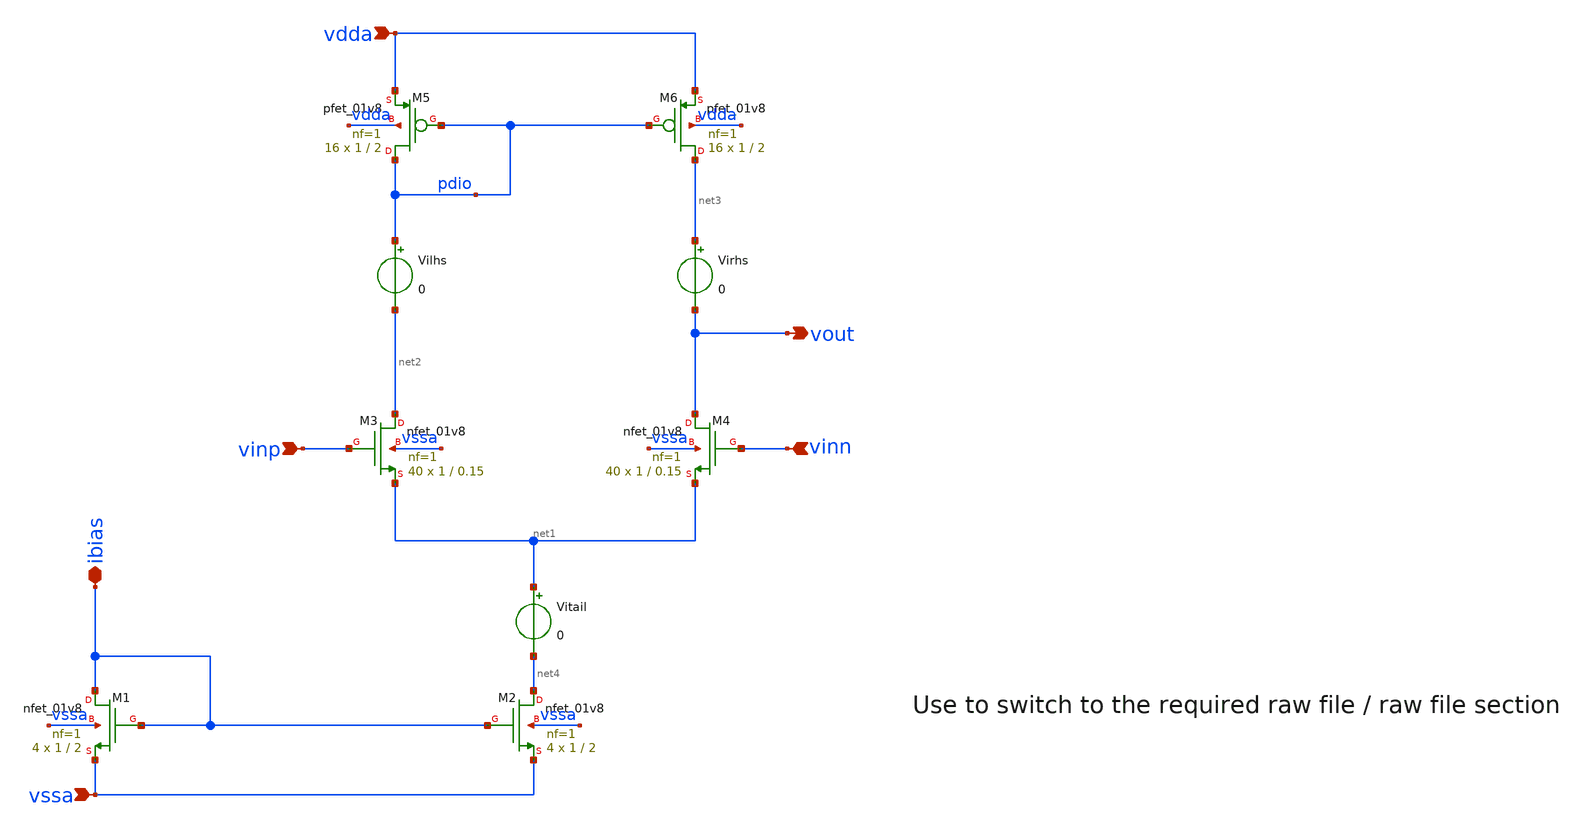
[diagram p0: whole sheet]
** sch_path: Analysing_DCOPs_in_xschem_ngpisce_in_SW130/OTA_DCOP2.sch
**.subckt OTA_DCOP2 ibias vdda vssa vinp vinn vout
*.iopin ibias
*.ipin vdda
*.ipin vssa
*.ipin vinp
*.ipin vinn
*.opin vout
XM3 net2 vinp net1 vssa sky130_fd_pr__nfet_01v8 L=0.15 W=1 nf=1 ad='int((nf+1)/2) * W/nf * 0.29' as='int((nf+2)/2) * W/nf * 0.29'
+ pd='2*int((nf+1)/2) * (W/nf + 0.29)' ps='2*int((nf+2)/2) * (W/nf + 0.29)' nrd='0.29 / W' nrs='0.29 / W'
+ sa=0 sb=0 sd=0 mult=40 m=40
XM4 vout vinn net1 vssa sky130_fd_pr__nfet_01v8 L=0.15 W=1 nf=1 ad='int((nf+1)/2) * W/nf * 0.29' as='int((nf+2)/2) * W/nf * 0.29'
+ pd='2*int((nf+1)/2) * (W/nf + 0.29)' ps='2*int((nf+2)/2) * (W/nf + 0.29)' nrd='0.29 / W' nrs='0.29 / W'
+ sa=0 sb=0 sd=0 mult=40 m=40
XM5 pdio pdio vdda vdda sky130_fd_pr__pfet_01v8 L=2 W=1 nf=1 ad='int((nf+1)/2) * W/nf * 0.29' as='int((nf+2)/2) * W/nf * 0.29'
+ pd='2*int((nf+1)/2) * (W/nf + 0.29)' ps='2*int((nf+2)/2) * (W/nf + 0.29)' nrd='0.29 / W' nrs='0.29 / W'
+ sa=0 sb=0 sd=0 mult=16 m=16
XM2 net4 ibias vssa vssa sky130_fd_pr__nfet_01v8 L=2 W=1 nf=1 ad='int((nf+1)/2) * W/nf * 0.29' as='int((nf+2)/2) * W/nf * 0.29'
+ pd='2*int((nf+1)/2) * (W/nf + 0.29)' ps='2*int((nf+2)/2) * (W/nf + 0.29)' nrd='0.29 / W' nrs='0.29 / W'
+ sa=0 sb=0 sd=0 mult=4 m=4
XM1 ibias ibias vssa vssa sky130_fd_pr__nfet_01v8 L=2 W=1 nf=1 ad='int((nf+1)/2) * W/nf * 0.29' as='int((nf+2)/2) * W/nf * 0.29'
+ pd='2*int((nf+1)/2) * (W/nf + 0.29)' ps='2*int((nf+2)/2) * (W/nf + 0.29)' nrd='0.29 / W' nrs='0.29 / W'
+ sa=0 sb=0 sd=0 mult=4 m=4
XM6 net3 pdio vdda vdda sky130_fd_pr__pfet_01v8 L=2 W=1 nf=1 ad='int((nf+1)/2) * W/nf * 0.29' as='int((nf+2)/2) * W/nf * 0.29'
+ pd='2*int((nf+1)/2) * (W/nf + 0.29)' ps='2*int((nf+2)/2) * (W/nf + 0.29)' nrd='0.29 / W' nrs='0.29 / W'
+ sa=0 sb=0 sd=0 mult=16 m=16
Vilhs pdio net2 0
Virhs net3 vout 0
Vitail net1 net4 0
**.ends
.end
